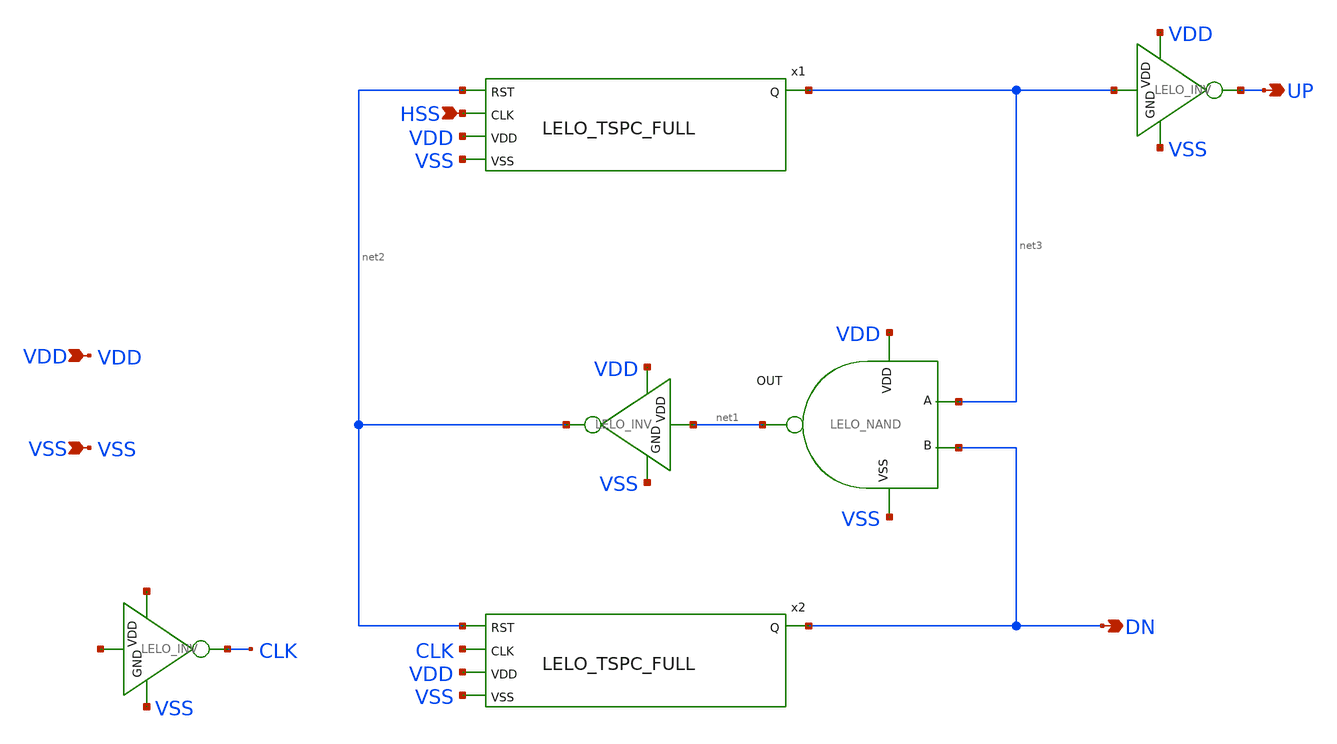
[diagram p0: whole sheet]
** sch_path: design/LELO_SVOD_SKY130A/LELO_pFD.sch
**.subckt LELO_pFD HSS UP DN VDD VSS
*.ipin HSS
*.opin UP
*.opin DN
*.ipin VDD
*.ipin VSS
x3 VDD net1 net3 DN VSS LELO_NAND
x4 VDD net1 net2 VSS LELO_INV
x1 net2 HSS VDD VSS net3 LELO_TSPC_FULL
x2 net2 CLK VDD VSS DN LELO_TSPC_FULL
x6 net4 net5 CLK VSS LELO_INV
x7 VDD net3 UP VSS LELO_INV
**.ends

* expanding   symbol:  LELO_SVOD_SKY130A/LELO_NAND.sym # of pins=5
** sym_path: design/LELO_SVOD_SKY130A/LELO_NAND.sym
** sch_path: design/LELO_SVOD_SKY130A/LELO_NAND.sch
.subckt LELO_NAND VDD OUT A B VSS
*.ipin VDD
*.ipin VSS
*.opin OUT
*.ipin A
*.ipin B
XM1 OUT B net1 net1 sky130_fd_pr__nfet_01v8_lvt L=0.15 W=1 nf=1 ad='int((1 + 1)/2) * 1 / 1 * 0.29' as='int((1 + 2)/2) * 1 / 1 * 0.29'
+ pd='2*int((1 + 1)/2) * (1 / 1 + 0.29)' ps='2*int((1 + 2)/2) * (1 / 1 + 0.29)' nrd='0.29 / 1 ' nrs='0.29 / 1 '
+ sa=0 sb=0 sd=0 mult=1 m=1
XM2 net1 A VSS VSS sky130_fd_pr__nfet_01v8_lvt L=0.15 W=1 nf=1 ad='int((1 + 1)/2) * 1 / 1 * 0.29' as='int((1 + 2)/2) * 1 / 1 * 0.29'
+ pd='2*int((1 + 1)/2) * (1 / 1 + 0.29)' ps='2*int((1 + 2)/2) * (1 / 1 + 0.29)' nrd='0.29 / 1 ' nrs='0.29 / 1 '
+ sa=0 sb=0 sd=0 mult=1 m=1
XM3 OUT A VDD VDD sky130_fd_pr__pfet_01v8_lvt L=0.35 W=1 nf=1 ad='int((1 + 1)/2) * 1 / 1 * 0.29' as='int((1 + 2)/2) * 1 / 1 * 0.29'
+ pd='2*int((1 + 1)/2) * (1 / 1 + 0.29)' ps='2*int((1 + 2)/2) * (1 / 1 + 0.29)' nrd='0.29 / 1 ' nrs='0.29 / 1 '
+ sa=0 sb=0 sd=0 mult=1 m=1
XM4 OUT B VDD net2 sky130_fd_pr__pfet_01v8_lvt L=0.35 W=1 nf=1 ad='int((1 + 1)/2) * 1 / 1 * 0.29' as='int((1 + 2)/2) * 1 / 1 * 0.29'
+ pd='2*int((1 + 1)/2) * (1 / 1 + 0.29)' ps='2*int((1 + 2)/2) * (1 / 1 + 0.29)' nrd='0.29 / 1 ' nrs='0.29 / 1 '
+ sa=0 sb=0 sd=0 mult=1 m=1
.ends


* expanding   symbol:  LELO_SVOD_SKY130A/LELO_INV.sym # of pins=4
** sym_path: design/LELO_SVOD_SKY130A/LELO_INV.sym
** sch_path: design/LELO_SVOD_SKY130A/LELO_INV.sch
.subckt LELO_INV VDD VIN VOUT GND
*.ipin VIN
*.ipin VDD
*.ipin GND
*.opin VOUT
XM1 VOUT VIN GND GND sky130_fd_pr__nfet_01v8_lvt L=0.35 W=0.42 nf=1 ad='int((1 + 1)/2) * 0.42 / 1 * 0.29'
+ as='int((1 + 2)/2) * 0.42 / 1 * 0.29' pd='2*int((1 + 1)/2) * (0.42 / 1 + 0.29)' ps='2*int((1 + 2)/2) * (0.42 / 1 + 0.29)'
+ nrd='0.29 / 0.42 ' nrs='0.29 / 0.42 ' sa=0 sb=0 sd=0 mult=1 m=1
XM2 VOUT VIN VDD VDD sky130_fd_pr__pfet_01v8_lvt L=0.35 W=1 nf=1 ad='int((1 + 1)/2) * 1 / 1 * 0.29' as='int((1 + 2)/2) * 1 / 1 * 0.29'
+ pd='2*int((1 + 1)/2) * (1 / 1 + 0.29)' ps='2*int((1 + 2)/2) * (1 / 1 + 0.29)' nrd='0.29 / 1 ' nrs='0.29 / 1 '
+ sa=0 sb=0 sd=0 mult=2 m=2
.ends


* expanding   symbol:  LELO_SVOD_SKY130A/LELO_TSPC_FULL.sym # of pins=5
** sym_path: design/LELO_SVOD_SKY130A/LELO_TSPC_FULL.sym
** sch_path: design/LELO_SVOD_SKY130A/LELO_TSPC_FULL.sch
.subckt LELO_TSPC_FULL RST CLK VDD VSS Q
*.ipin RST
*.ipin CLK
*.ipin VDD
*.ipin VSS
*.opin Q
XM1 net2 RST VSS VSS sky130_fd_pr__nfet_01v8_lvt L=0.15 W=1 nf=1 ad='int((1 + 1)/2) * 1 / 1 * 0.29' as='int((1 + 2)/2) * 1 / 1 * 0.29'
+ pd='2*int((1 + 1)/2) * (1 / 1 + 0.29)' ps='2*int((1 + 2)/2) * (1 / 1 + 0.29)' nrd='0.29 / 1 ' nrs='0.29 / 1 '
+ sa=0 sb=0 sd=0 mult=1 m=1
XM2 net2 CLK net1 VDD sky130_fd_pr__pfet_01v8_lvt L=0.35 W=4 nf=1 ad='int((1 + 1)/2) * 4 / 1 * 0.29'
+ as='int((1 + 2)/2) * 4 / 1 * 0.29' pd='2*int((1 + 1)/2) * (4 / 1 + 0.29)' ps='2*int((1 + 2)/2) * (4 / 1 + 0.29)'
+ nrd='0.29 / 4 ' nrs='0.29 / 4 ' sa=0 sb=0 sd=0 mult=1 m=1
XM3 net1 RST VDD VDD sky130_fd_pr__pfet_01v8_lvt L=0.35 W=4 nf=1 ad='int((1 + 1)/2) * 4 / 1 * 0.29' as='int((1 + 2)/2) * 4 / 1 * 0.29'
+ pd='2*int((1 + 1)/2) * (4 / 1 + 0.29)' ps='2*int((1 + 2)/2) * (4 / 1 + 0.29)' nrd='0.29 / 4 ' nrs='0.29 / 4 '
+ sa=0 sb=0 sd=0 mult=1 m=1
XM4 net3 net2 VSS VSS sky130_fd_pr__nfet_01v8_lvt L=0.15 W=4 nf=1 ad='int((1 + 1)/2) * 4 / 1 * 0.29'
+ as='int((1 + 2)/2) * 4 / 1 * 0.29' pd='2*int((1 + 1)/2) * (4 / 1 + 0.29)' ps='2*int((1 + 2)/2) * (4 / 1 + 0.29)'
+ nrd='0.29 / 4 ' nrs='0.29 / 4 ' sa=0 sb=0 sd=0 mult=1 m=1
XM5 Q_B CLK net3 net3 sky130_fd_pr__nfet_01v8_lvt L=0.15 W=4 nf=1 ad='int((1 + 1)/2) * 4 / 1 * 0.29'
+ as='int((1 + 2)/2) * 4 / 1 * 0.29' pd='2*int((1 + 1)/2) * (4 / 1 + 0.29)' ps='2*int((1 + 2)/2) * (4 / 1 + 0.29)'
+ nrd='0.29 / 4 ' nrs='0.29 / 4 ' sa=0 sb=0 sd=0 mult=1 m=1
XM6 Q_B net2 VDD VDD sky130_fd_pr__pfet_01v8_lvt L=0.35 W=4 nf=1 ad='int((1 + 1)/2) * 4 / 1 * 0.29' as='int((1 + 2)/2) * 4 / 1 * 0.29'
+ pd='2*int((1 + 1)/2) * (4 / 1 + 0.29)' ps='2*int((1 + 2)/2) * (4 / 1 + 0.29)' nrd='0.29 / 4 ' nrs='0.29 / 4 '
+ sa=0 sb=0 sd=0 mult=1 m=1
XM7 Q Q_B VSS VSS sky130_fd_pr__nfet_01v8_lvt L=0.15 W=0.5 nf=1 ad='int((1 + 1)/2) * 0.5 / 1 * 0.29'
+ as='int((1 + 2)/2) * 0.5 / 1 * 0.29' pd='2*int((1 + 1)/2) * (0.5 / 1 + 0.29)' ps='2*int((1 + 2)/2) * (0.5 / 1 + 0.29)'
+ nrd='0.29 / 0.5 ' nrs='0.29 / 0.5 ' sa=0 sb=0 sd=0 mult=1 m=1
XM8 Q Q_B VDD VDD sky130_fd_pr__pfet_01v8_lvt L=0.35 W=2 nf=1 ad='int((1 + 1)/2) * 2 / 1 * 0.29' as='int((1 + 2)/2) * 2 / 1 * 0.29'
+ pd='2*int((1 + 1)/2) * (2 / 1 + 0.29)' ps='2*int((1 + 2)/2) * (2 / 1 + 0.29)' nrd='0.29 / 2 ' nrs='0.29 / 2 '
+ sa=0 sb=0 sd=0 mult=1 m=1
.ends

.end
